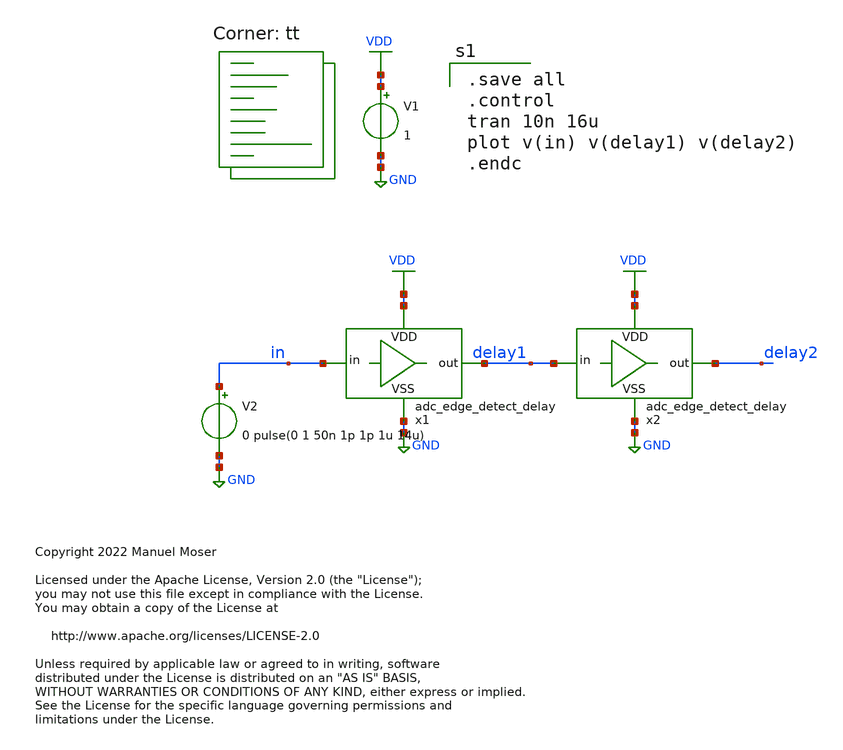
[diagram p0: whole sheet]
** sch_path: xschem/adc_edge_detect_delay/adc_edge_detect_delay_tb.sch
* Copyright 2022 Manuel Moser
* Licensed under the Apache License, Version 2.0 (the "License");
**.subckt adc_edge_detect_delay_tb
x1 VDD in delay1 GND adc_edge_detect_delay
x2 VDD delay1 delay2 GND adc_edge_detect_delay
V1 VDD GND 1
V2 in GND 0 pulse(0 1 50n 1p 1p 1u 14u)
**** begin user architecture code

.save all
.control
tran 10n 16u
plot v(in) v(delay1) v(delay2)
.endc

.lib $::SKYWATER_MODELS/sky130.lib.spice tt
**** end user architecture code
**.ends
.GLOBAL VDD
.GLOBAL GND
.end
